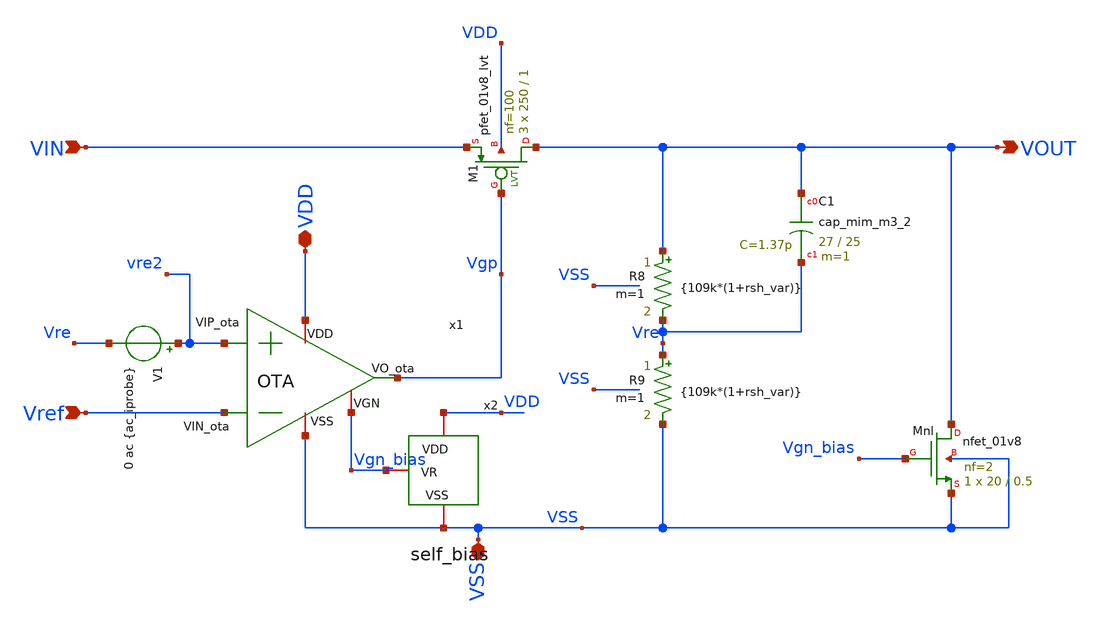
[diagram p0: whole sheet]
** sch_path: xschem/LDO.sch
**.subckt LDO VIN VDD VOUT Vref VSS
*.ipin VIN
*.iopin VDD
*.opin VOUT
*.ipin Vref
*.iopin VSS
V1 vre2 Vre 0 ac {ac_iprobe}
x1 VDD Vgp Vref vre2 VSS Vgn_bias OTA
XC1 VOUT Vre sky130_fd_pr__cap_mim_m3_2 W=27 L=25 MF=1 m=1
XM1 VOUT Vgp VIN VDD sky130_fd_pr__pfet_01v8_lvt L=1 W=250 nf=100 ad='int((100 + 1)/2) * 250 / 100 * 0.29'
+ as='int((100 + 2)/2) * 250 / 100 * 0.29' pd='2*int((100 + 1)/2) * (250 / 100 + 0.29)' ps='2*int((100 + 2)/2) * (250 / 100 + 0.29)'
+ nrd='0.29 / 250 ' nrs='0.29 / 250 ' sa=0 sb=0 sd=0 mult=3 m=3
x2 VDD Vgn_bias VSS self_bias
XMnl VOUT Vgn_bias VSS VSS sky130_fd_pr__nfet_01v8 L=0.5 W=20 nf=2 ad='int((2 + 1)/2) * 20 / 2 * 0.29'
+ as='int((2 + 2)/2) * 20 / 2 * 0.29' pd='2*int((2 + 1)/2) * (20 / 2 + 0.29)' ps='2*int((2 + 2)/2) * (20 / 2 + 0.29)'
+ nrd='0.29 / 20 ' nrs='0.29 / 20 ' sa=0 sb=0 sd=0 mult=1 m=1
R8 VOUT Vre {109k*(1+rsh_var)} m=1
R9 Vre VSS {109k*(1+rsh_var)} m=1
**.ends

* expanding   symbol:  /foss/designs/LDO-sky130/xschem/OTA.sym # of pins=6
** sym_path: xschem/OTA/OTA.sym
** sch_path: xschem/OTA/OTA.sch
.subckt OTA VDD VO_ota VIN_ota VIP_ota VSS VGN
*.ipin VIN_ota
*.opin VO_ota
*.iopin VSS
*.iopin VDD
*.ipin VIP_ota
*.iopin VGN
XMpr vo1 vd VSS VSS sky130_fd_pr__nfet_01v8 L=1 W=6 nf=4 ad='int((4 + 1)/2) * 6 / 4 * 0.29' as='int((4 + 2)/2) * 6 / 4 * 0.29'
+ pd='2*int((4 + 1)/2) * (6 / 4 + 0.29)' ps='2*int((4 + 2)/2) * (6 / 4 + 0.29)' nrd='0.29 / 6 ' nrs='0.29 / 6 '
+ sa=0 sb=0 sd=0 mult=1 m=1
XMnr vd vd VSS VSS sky130_fd_pr__nfet_01v8 L=1 W=6 nf=4 ad='int((4 + 1)/2) * 6 / 4 * 0.29' as='int((4 + 2)/2) * 6 / 4 * 0.29'
+ pd='2*int((4 + 1)/2) * (6 / 4 + 0.29)' ps='2*int((4 + 2)/2) * (6 / 4 + 0.29)' nrd='0.29 / 6 ' nrs='0.29 / 6 '
+ sa=0 sb=0 sd=0 mult=1 m=1
XMo VO_ota vo1 VSS VSS sky130_fd_pr__nfet_01v8 L=2 W=8 nf=8 ad='int((8 + 1)/2) * 8 / 8 * 0.29' as='int((8 + 2)/2) * 8 / 8 * 0.29'
+ pd='2*int((8 + 1)/2) * (8 / 8 + 0.29)' ps='2*int((8 + 2)/2) * (8 / 8 + 0.29)' nrd='0.29 / 8 ' nrs='0.29 / 8 '
+ sa=0 sb=0 sd=0 mult=1 m=1
XMrc2 VO_ota vgp VDD VDD sky130_fd_pr__pfet_01v8_lvt L=2 W=50 nf=8 ad='int((8 + 1)/2) * 50 / 8 * 0.29'
+ as='int((8 + 2)/2) * 50 / 8 * 0.29' pd='2*int((8 + 1)/2) * (50 / 8 + 0.29)' ps='2*int((8 + 2)/2) * (50 / 8 + 0.29)'
+ nrd='0.29 / 50 ' nrs='0.29 / 50 ' sa=0 sb=0 sd=0 mult=1 m=1
XC1 VO_ota vmiler sky130_fd_pr__cap_mim_m3_2 W=44.6 L=56 MF=1 m=1
XMp vo1 VIP_ota vtail VDD sky130_fd_pr__pfet_01v8_lvt L=1 W=26 nf=4 ad='int((4 + 1)/2) * 26 / 4 * 0.29'
+ as='int((4 + 2)/2) * 26 / 4 * 0.29' pd='2*int((4 + 1)/2) * (26 / 4 + 0.29)' ps='2*int((4 + 2)/2) * (26 / 4 + 0.29)'
+ nrd='0.29 / 26 ' nrs='0.29 / 26 ' sa=0 sb=0 sd=0 mult=1 m=1
XMn vd VIN_ota vtail VDD sky130_fd_pr__pfet_01v8_lvt L=1 W=26 nf=4 ad='int((4 + 1)/2) * 26 / 4 * 0.29'
+ as='int((4 + 2)/2) * 26 / 4 * 0.29' pd='2*int((4 + 1)/2) * (26 / 4 + 0.29)' ps='2*int((4 + 2)/2) * (26 / 4 + 0.29)'
+ nrd='0.29 / 26 ' nrs='0.29 / 26 ' sa=0 sb=0 sd=0 mult=1 m=1
XMrc1 vtail vgp VDD VDD sky130_fd_pr__pfet_01v8_lvt L=1 W=50 nf=8 ad='int((8 + 1)/2) * 50 / 8 * 0.29'
+ as='int((8 + 2)/2) * 50 / 8 * 0.29' pd='2*int((8 + 1)/2) * (50 / 8 + 0.29)' ps='2*int((8 + 2)/2) * (50 / 8 + 0.29)'
+ nrd='0.29 / 50 ' nrs='0.29 / 50 ' sa=0 sb=0 sd=0 mult=1 m=1
XMr vgp vgp VDD VDD sky130_fd_pr__pfet_01v8_lvt L=1 W=12.5 nf=2 ad='int((2 + 1)/2) * 12.5 / 2 * 0.29'
+ as='int((2 + 2)/2) * 12.5 / 2 * 0.29' pd='2*int((2 + 1)/2) * (12.5 / 2 + 0.29)' ps='2*int((2 + 2)/2) * (12.5 / 2 + 0.29)'
+ nrd='0.29 / 12.5 ' nrs='0.29 / 12.5 ' sa=0 sb=0 sd=0 mult=1 m=1
XMnref vgp VGN VSS VSS sky130_fd_pr__nfet_01v8 L=1 W=8 nf=1 ad='int((1 + 1)/2) * 8 / 1 * 0.29' as='int((1 + 2)/2) * 8 / 1 * 0.29'
+ pd='2*int((1 + 1)/2) * (8 / 1 + 0.29)' ps='2*int((1 + 2)/2) * (8 / 1 + 0.29)' nrd='0.29 / 8 ' nrs='0.29 / 8 '
+ sa=0 sb=0 sd=0 mult=1 m=1
XR10 vo1 vmiler VSS sky130_fd_pr__res_xhigh_po_0p35 L=90.72 mult=1 m=1
.ends


* expanding   symbol:  /foss/designs/OSCAR/xschem/Iref/self_bias.sym # of pins=3
** sym_path: xschem/Iref/self_bias.sym
** sch_path: xschem/Iref/self_bias.sch
.subckt self_bias VDD VR VSS
*.iopin VR
*.iopin VDD
*.iopin VSS
XMp4 vgp_self vgp_self VDD VDD sky130_fd_pr__pfet_01v8_lvt L=1 W=30 nf=6 ad='int((6 + 1)/2) * 30 / 6 * 0.29'
+ as='int((6 + 2)/2) * 30 / 6 * 0.29' pd='2*int((6 + 1)/2) * (30 / 6 + 0.29)' ps='2*int((6 + 2)/2) * (30 / 6 + 0.29)'
+ nrd='0.29 / 30 ' nrs='0.29 / 30 ' sa=0 sb=0 sd=0 mult=1 m=1
XMp3 VDI vgp_self VDD VDD sky130_fd_pr__pfet_01v8_lvt L=1 W=30 nf=6 ad='int((6 + 1)/2) * 30 / 6 * 0.29'
+ as='int((6 + 2)/2) * 30 / 6 * 0.29' pd='2*int((6 + 1)/2) * (30 / 6 + 0.29)' ps='2*int((6 + 2)/2) * (30 / 6 + 0.29)'
+ nrd='0.29 / 30 ' nrs='0.29 / 30 ' sa=0 sb=0 sd=0 mult=1 m=1
XMs2 VDinv VR vp1 VDD sky130_fd_pr__pfet_01v8_lvt L=5 W=0.5 nf=1 ad='int((1 + 1)/2) * 0.5 / 1 * 0.29'
+ as='int((1 + 2)/2) * 0.5 / 1 * 0.29' pd='2*int((1 + 1)/2) * (0.5 / 1 + 0.29)' ps='2*int((1 + 2)/2) * (0.5 / 1 + 0.29)'
+ nrd='0.29 / 0.5 ' nrs='0.29 / 0.5 ' sa=0 sb=0 sd=0 mult=1 m=1
XMn2 vgp_self VDI VR VSS sky130_fd_pr__nfet_01v8 L=1 W=24 nf=6 ad='int((6 + 1)/2) * 24 / 6 * 0.29' as='int((6 + 2)/2) * 24 / 6 * 0.29'
+ pd='2*int((6 + 1)/2) * (24 / 6 + 0.29)' ps='2*int((6 + 2)/2) * (24 / 6 + 0.29)' nrd='0.29 / 24 ' nrs='0.29 / 24 '
+ sa=0 sb=0 sd=0 mult=1 m=1
XMn1 VDI VR VSS VSS sky130_fd_pr__nfet_01v8 L=1 W=5 nf=5 ad='int((5 + 1)/2) * 5 / 5 * 0.29' as='int((5 + 2)/2) * 5 / 5 * 0.29'
+ pd='2*int((5 + 1)/2) * (5 / 5 + 0.29)' ps='2*int((5 + 2)/2) * (5 / 5 + 0.29)' nrd='0.29 / 5 ' nrs='0.29 / 5 '
+ sa=0 sb=0 sd=0 mult=1 m=1
XMs3 VDinv VR VSS VSS sky130_fd_pr__nfet_01v8 L=1 W=20 nf=5 ad='int((5 + 1)/2) * 20 / 5 * 0.29' as='int((5 + 2)/2) * 20 / 5 * 0.29'
+ pd='2*int((5 + 1)/2) * (20 / 5 + 0.29)' ps='2*int((5 + 2)/2) * (20 / 5 + 0.29)' nrd='0.29 / 20 ' nrs='0.29 / 20 '
+ sa=0 sb=0 sd=0 mult=1 m=1
XMs1 vgp_self VDinv VSS VSS sky130_fd_pr__nfet_01v8 L=1 W=2 nf=2 ad='int((2 + 1)/2) * 2 / 2 * 0.29' as='int((2 + 2)/2) * 2 / 2 * 0.29'
+ pd='2*int((2 + 1)/2) * (2 / 2 + 0.29)' ps='2*int((2 + 2)/2) * (2 / 2 + 0.29)' nrd='0.29 / 2 ' nrs='0.29 / 2 '
+ sa=0 sb=0 sd=0 mult=1 m=1
XR11 VSS VR VSS sky130_fd_pr__res_xhigh_po_0p69 L=20.7 mult=1 m=1
XMs4 vp1 VR vp2 VDD sky130_fd_pr__pfet_01v8_lvt L=5 W=0.5 nf=1 ad='int((1 + 1)/2) * 0.5 / 1 * 0.29' as='int((1 + 2)/2) * 0.5 / 1 * 0.29'
+ pd='2*int((1 + 1)/2) * (0.5 / 1 + 0.29)' ps='2*int((1 + 2)/2) * (0.5 / 1 + 0.29)' nrd='0.29 / 0.5 ' nrs='0.29 / 0.5 '
+ sa=0 sb=0 sd=0 mult=1 m=1
XMs5 vp2 VR vp3 VDD sky130_fd_pr__pfet_01v8_lvt L=5 W=0.5 nf=1 ad='int((1 + 1)/2) * 0.5 / 1 * 0.29' as='int((1 + 2)/2) * 0.5 / 1 * 0.29'
+ pd='2*int((1 + 1)/2) * (0.5 / 1 + 0.29)' ps='2*int((1 + 2)/2) * (0.5 / 1 + 0.29)' nrd='0.29 / 0.5 ' nrs='0.29 / 0.5 '
+ sa=0 sb=0 sd=0 mult=1 m=1
XMs6 vp3 VR vp4 VDD sky130_fd_pr__pfet_01v8_lvt L=5 W=0.5 nf=1 ad='int((1 + 1)/2) * 0.5 / 1 * 0.29' as='int((1 + 2)/2) * 0.5 / 1 * 0.29'
+ pd='2*int((1 + 1)/2) * (0.5 / 1 + 0.29)' ps='2*int((1 + 2)/2) * (0.5 / 1 + 0.29)' nrd='0.29 / 0.5 ' nrs='0.29 / 0.5 '
+ sa=0 sb=0 sd=0 mult=1 m=1
XMs7 vp4 VR VDD VDD sky130_fd_pr__pfet_01v8_lvt L=5 W=0.5 nf=1 ad='int((1 + 1)/2) * 0.5 / 1 * 0.29' as='int((1 + 2)/2) * 0.5 / 1 * 0.29'
+ pd='2*int((1 + 1)/2) * (0.5 / 1 + 0.29)' ps='2*int((1 + 2)/2) * (0.5 / 1 + 0.29)' nrd='0.29 / 0.5 ' nrs='0.29 / 0.5 '
+ sa=0 sb=0 sd=0 mult=1 m=1
.ends

.end
